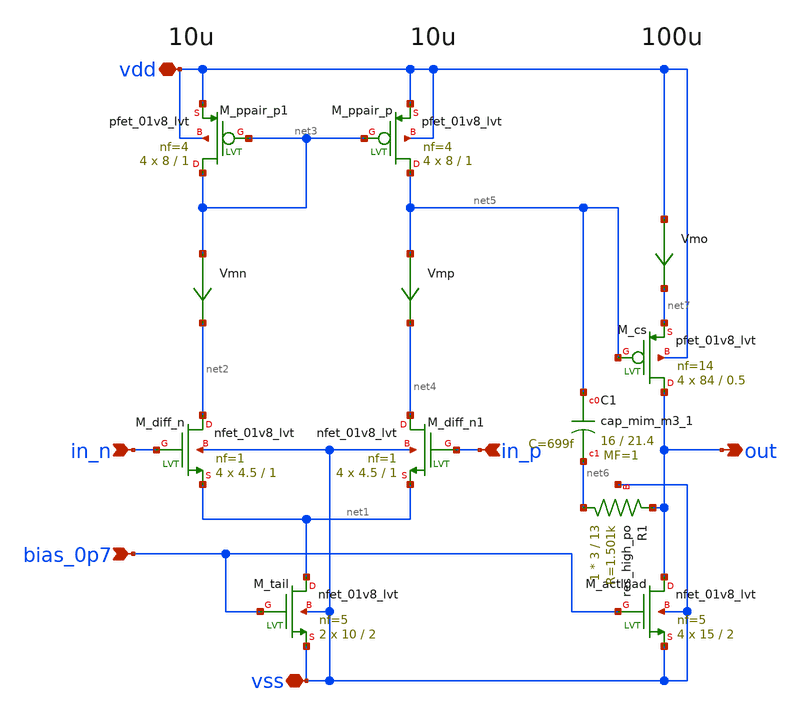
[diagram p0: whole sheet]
** sch_path: design/opamp/opamp_realcomp3_meas_current.sch
**.subckt opamp_realcomp3_meas_current vdd vss in_n in_p out bias_0p7
*.iopin vdd
*.iopin vss
*.ipin in_n
*.ipin in_p
*.opin out
*.ipin bias_0p7
XM_diff_n net2 in_n net1 vss sky130_fd_pr__nfet_01v8_lvt L=1 W=4.5 nf=1 ad='int((nf+1)/2) * W/nf * 0.29'
+ as='int((nf+2)/2) * W/nf * 0.29' pd='2*int((nf+1)/2) * (W/nf + 0.29)' ps='2*int((nf+2)/2) * (W/nf + 0.29)'
+ nrd='0.29 / W' nrs='0.29 / W' sa=0 sb=0 sd=0 mult=4 m=4
XM_diff_n1 net4 in_p net1 vss sky130_fd_pr__nfet_01v8_lvt L=1 W=4.5 nf=1 ad='int((nf+1)/2) * W/nf * 0.29'
+ as='int((nf+2)/2) * W/nf * 0.29' pd='2*int((nf+1)/2) * (W/nf + 0.29)' ps='2*int((nf+2)/2) * (W/nf + 0.29)'
+ nrd='0.29 / W' nrs='0.29 / W' sa=0 sb=0 sd=0 mult=4 m=4
XM_tail net1 bias_0p7 vss vss sky130_fd_pr__nfet_01v8_lvt L=2 W=10 nf=5 ad='int((nf+1)/2) * W/nf * 0.29'
+ as='int((nf+2)/2) * W/nf * 0.29' pd='2*int((nf+1)/2) * (W/nf + 0.29)' ps='2*int((nf+2)/2) * (W/nf + 0.29)'
+ nrd='0.29 / W' nrs='0.29 / W' sa=0 sb=0 sd=0 mult=2 m=2
XM_actload out bias_0p7 vss vss sky130_fd_pr__nfet_01v8_lvt L=2 W=15 nf=5 ad='int((nf+1)/2) * W/nf * 0.29'
+ as='int((nf+2)/2) * W/nf * 0.29' pd='2*int((nf+1)/2) * (W/nf + 0.29)' ps='2*int((nf+2)/2) * (W/nf + 0.29)'
+ nrd='0.29 / W' nrs='0.29 / W' sa=0 sb=0 sd=0 mult=4 m=4
XM_ppair_p net5 net3 vdd vdd sky130_fd_pr__pfet_01v8_lvt L=1 W=8 nf=4 ad='int((nf+1)/2) * W/nf * 0.29'
+ as='int((nf+2)/2) * W/nf * 0.29' pd='2*int((nf+1)/2) * (W/nf + 0.29)' ps='2*int((nf+2)/2) * (W/nf + 0.29)'
+ nrd='0.29 / W' nrs='0.29 / W' sa=0 sb=0 sd=0 mult=4 m=4
XM_ppair_p1 net3 net3 vdd vdd sky130_fd_pr__pfet_01v8_lvt L=1 W=8 nf=4 ad='int((nf+1)/2) * W/nf * 0.29'
+ as='int((nf+2)/2) * W/nf * 0.29' pd='2*int((nf+1)/2) * (W/nf + 0.29)' ps='2*int((nf+2)/2) * (W/nf + 0.29)'
+ nrd='0.29 / W' nrs='0.29 / W' sa=0 sb=0 sd=0 mult=4 m=4
XM_cs out net5 net7 vdd sky130_fd_pr__pfet_01v8_lvt L=0.5 W=84 nf=14 ad='int((nf+1)/2) * W/nf * 0.29'
+ as='int((nf+2)/2) * W/nf * 0.29' pd='2*int((nf+1)/2) * (W/nf + 0.29)' ps='2*int((nf+2)/2) * (W/nf + 0.29)'
+ nrd='0.29 / W' nrs='0.29 / W' sa=0 sb=0 sd=0 mult=4 m=4
XR1 net6 out vss sky130_fd_pr__res_high_po W=3 L=13 mult=1 m=1
XC1 net5 net6 sky130_fd_pr__cap_mim_m3_1 W=16 L=21.4 MF=1 m=1
Vmn net3 net2 0
.save i(vmn)
Vmp net5 net4 0
.save i(vmp)
Vmo vdd net7 0
.save i(vmo)
**.ends
.end
